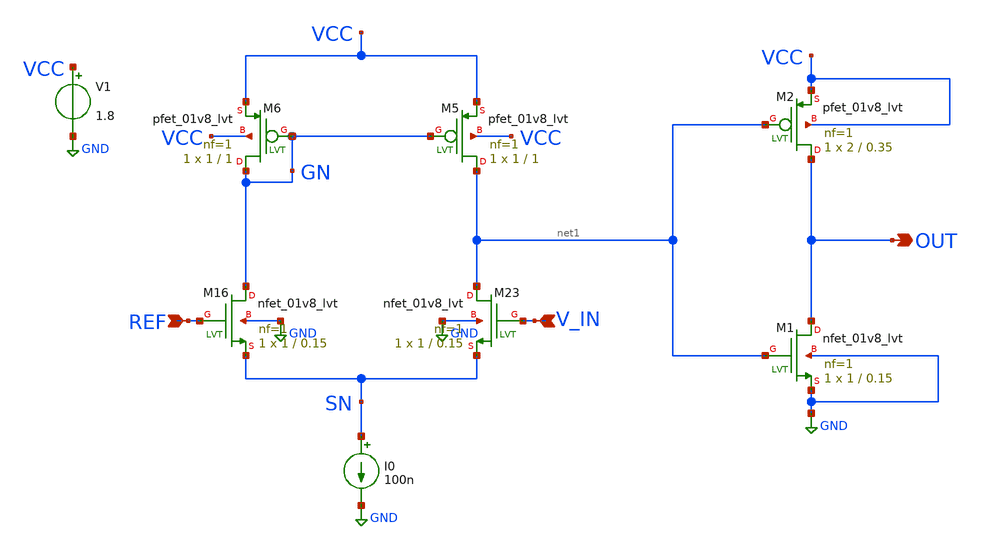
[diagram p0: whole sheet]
** sch_path: xschem/comp.sch
**.subckt comp REF V_IN OUT
*.ipin REF
*.ipin V_IN
*.opin OUT
XM5 net1 GN VCC VCC sky130_fd_pr__pfet_01v8_lvt L=1 W=1 nf=1 ad='W * 0.29' as='W * 0.29' pd='2*(W + 0.29)'
+ ps='2*(W + 0.29)' nrd=0 nrs=0 sa=0 sb=0 sd=0 mult=1 m=1
XM6 GN GN VCC VCC sky130_fd_pr__pfet_01v8_lvt L=1 W=1 nf=1 ad='W * 0.29' as='W * 0.29' pd='2*(W + 0.29)'
+ ps='2*(W + 0.29)' nrd=0 nrs=0 sa=0 sb=0 sd=0 mult=1 m=1
XM23 net1 V_IN SN GND sky130_fd_pr__nfet_01v8_lvt L=0.15 W=1 nf=1 ad='W * 0.29' as='W * 0.29' pd='2*(W + 0.29)'
+ ps='2*(W + 0.29)' nrd=0 nrs=0 sa=0 sb=0 sd=0 mult=1 m=1
XM16 GN REF SN GND sky130_fd_pr__nfet_01v8_lvt L=0.15 W=1 nf=1 ad='W * 0.29' as='W * 0.29' pd='2*(W + 0.29)'
+ ps='2*(W + 0.29)' nrd=0 nrs=0 sa=0 sb=0 sd=0 mult=1 m=1
I0 SN GND 100n
XM1 OUT net1 GND GND sky130_fd_pr__nfet_01v8_lvt L=0.15 W=1 nf=1 ad='W * 0.29' as='W * 0.29' pd='2*(W + 0.29)'
+ ps='2*(W + 0.29)' nrd=0 nrs=0 sa=0 sb=0 sd=0 mult=1 m=1
XM2 OUT net1 VCC VCC sky130_fd_pr__pfet_01v8_lvt L=0.35 W=2 nf=1 ad='W * 0.29' as='W * 0.29' pd='2*(W + 0.29)'
+ ps='2*(W + 0.29)' nrd=0 nrs=0 sa=0 sb=0 sd=0 mult=1 m=1
V1 VCC GND 1.8
**.ends
.GLOBAL GND
.end
